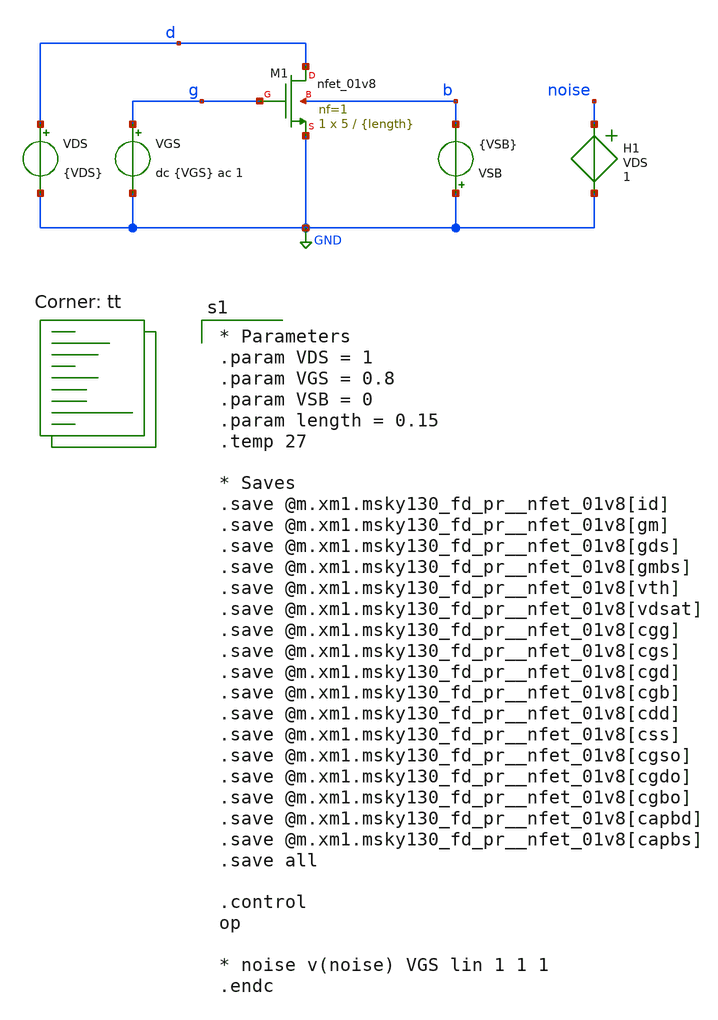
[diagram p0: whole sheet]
** sch_path: analog/gm-ID-LUT/schematics/sweep_nfet_01v8.sch
**.subckt sweep_nfet_01v8
XM1 d g GND b sky130_fd_pr__nfet_01v8 L={length} W=5 nf=1 ad='int((nf+1)/2) * W/nf * 0.29' as='int((nf+2)/2) * W/nf * 0.29'
+ pd='2*int((nf+1)/2) * (W/nf + 0.29)' ps='2*int((nf+2)/2) * (W/nf + 0.29)' nrd='0.29 / W' nrs='0.29 / W'
+ sa=0 sb=0 sd=0 mult=1 m=1
VDS d GND {VDS}
VGS g GND dc {VGS} ac 1
VSB GND b {VSB}
H1 noise GND VDS 1
**** begin user architecture code
.lib $::SKYWATER_MODELS/sky130.lib.spice tt

* Parameters
.param VDS = 1
.param VGS = 0.8
.param VSB = 0
.param length = 0.15
.temp 27

* Saves
.save @m.xm1.msky130_fd_pr__nfet_01v8[id]
.save @m.xm1.msky130_fd_pr__nfet_01v8[gm]
.save @m.xm1.msky130_fd_pr__nfet_01v8[gds]
.save @m.xm1.msky130_fd_pr__nfet_01v8[gmbs]
.save @m.xm1.msky130_fd_pr__nfet_01v8[vth]
.save @m.xm1.msky130_fd_pr__nfet_01v8[vdsat]
.save @m.xm1.msky130_fd_pr__nfet_01v8[cgg]
.save @m.xm1.msky130_fd_pr__nfet_01v8[cgs]
.save @m.xm1.msky130_fd_pr__nfet_01v8[cgd]
.save @m.xm1.msky130_fd_pr__nfet_01v8[cgb]
.save @m.xm1.msky130_fd_pr__nfet_01v8[cdd]
.save @m.xm1.msky130_fd_pr__nfet_01v8[css]
.save @m.xm1.msky130_fd_pr__nfet_01v8[cgso]
.save @m.xm1.msky130_fd_pr__nfet_01v8[cgdo]
.save @m.xm1.msky130_fd_pr__nfet_01v8[cgbo]
.save @m.xm1.msky130_fd_pr__nfet_01v8[capbd]
.save @m.xm1.msky130_fd_pr__nfet_01v8[capbs]
.save all

.control
op

* noise v(noise) VGS lin 1 1 1
.endc


**** end user architecture code
**.ends
.GLOBAL GND
.end
